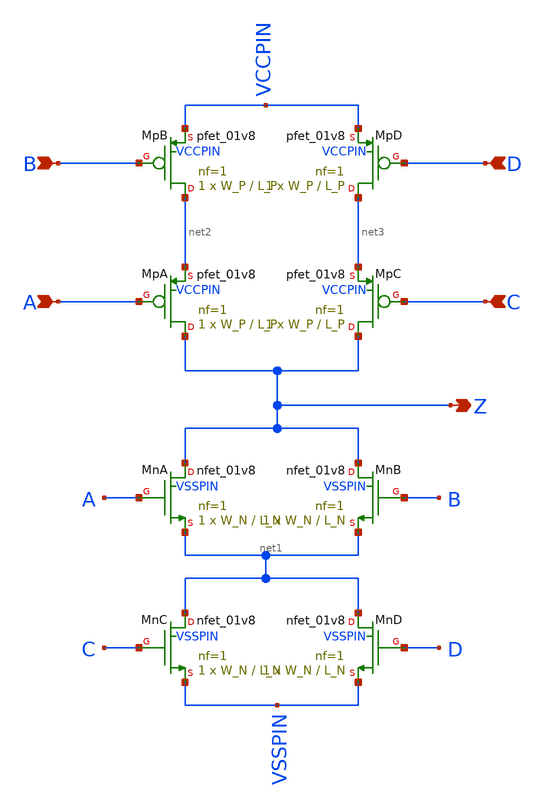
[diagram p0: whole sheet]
** sch_path: skywater-tests/A2O2O2I1.sch
**.subckt A2O2O2I1 B Z A D C
*.ipin B
*.opin Z
*.ipin A
*.ipin D
*.ipin C
XMnA Z A net1 VSSPIN sky130_fd_pr__nfet_01v8 L=L_N W=W_N nf=1 ad='int((nf+1)/2) * W/nf * 0.29' as='int((nf+2)/2) * W/nf * 0.29'
+ pd='2*int((nf+1)/2) * (W/nf + 0.29)' ps='2*int((nf+2)/2) * (W/nf + 0.29)' nrd='0.29 / W' nrs='0.29 / W'
+ sa=0 sb=0 sd=0 mult=1 m=1
XMpB net2 B VCCPIN VCCPIN sky130_fd_pr__pfet_01v8 L=L_P W=W_P nf=1 ad='int((nf+1)/2) * W/nf * 0.29' as='int((nf+2)/2) * W/nf * 0.29'
+ pd='2*int((nf+1)/2) * (W/nf + 0.29)' ps='2*int((nf+2)/2) * (W/nf + 0.29)' nrd='0.29 / W' nrs='0.29 / W'
+ sa=0 sb=0 sd=0 mult=1 m=1
XMnB Z B net1 VSSPIN sky130_fd_pr__nfet_01v8 L=L_N W=W_N nf=1 ad='int((nf+1)/2) * W/nf * 0.29' as='int((nf+2)/2) * W/nf * 0.29'
+ pd='2*int((nf+1)/2) * (W/nf + 0.29)' ps='2*int((nf+2)/2) * (W/nf + 0.29)' nrd='0.29 / W' nrs='0.29 / W'
+ sa=0 sb=0 sd=0 mult=1 m=1
XMnC net1 C VSSPIN VSSPIN sky130_fd_pr__nfet_01v8 L=L_N W=W_N nf=1 ad='int((nf+1)/2) * W/nf * 0.29' as='int((nf+2)/2) * W/nf * 0.29'
+ pd='2*int((nf+1)/2) * (W/nf + 0.29)' ps='2*int((nf+2)/2) * (W/nf + 0.29)' nrd='0.29 / W' nrs='0.29 / W'
+ sa=0 sb=0 sd=0 mult=1 m=1
XMnD net1 D VSSPIN VSSPIN sky130_fd_pr__nfet_01v8 L=L_N W=W_N nf=1 ad='int((nf+1)/2) * W/nf * 0.29' as='int((nf+2)/2) * W/nf * 0.29'
+ pd='2*int((nf+1)/2) * (W/nf + 0.29)' ps='2*int((nf+2)/2) * (W/nf + 0.29)' nrd='0.29 / W' nrs='0.29 / W'
+ sa=0 sb=0 sd=0 mult=1 m=1
XMpA Z A net2 VCCPIN sky130_fd_pr__pfet_01v8 L=L_P W=W_P nf=1 ad='int((nf+1)/2) * W/nf * 0.29' as='int((nf+2)/2) * W/nf * 0.29'
+ pd='2*int((nf+1)/2) * (W/nf + 0.29)' ps='2*int((nf+2)/2) * (W/nf + 0.29)' nrd='0.29 / W' nrs='0.29 / W'
+ sa=0 sb=0 sd=0 mult=1 m=1
XMpD net3 D VCCPIN VCCPIN sky130_fd_pr__pfet_01v8 L=L_P W=W_P nf=1 ad='int((nf+1)/2) * W/nf * 0.29' as='int((nf+2)/2) * W/nf * 0.29'
+ pd='2*int((nf+1)/2) * (W/nf + 0.29)' ps='2*int((nf+2)/2) * (W/nf + 0.29)' nrd='0.29 / W' nrs='0.29 / W'
+ sa=0 sb=0 sd=0 mult=1 m=1
XMpC Z C net3 VCCPIN sky130_fd_pr__pfet_01v8 L=L_P W=W_P nf=1 ad='int((nf+1)/2) * W/nf * 0.29' as='int((nf+2)/2) * W/nf * 0.29'
+ pd='2*int((nf+1)/2) * (W/nf + 0.29)' ps='2*int((nf+2)/2) * (W/nf + 0.29)' nrd='0.29 / W' nrs='0.29 / W'
+ sa=0 sb=0 sd=0 mult=1 m=1
**.ends
.end
